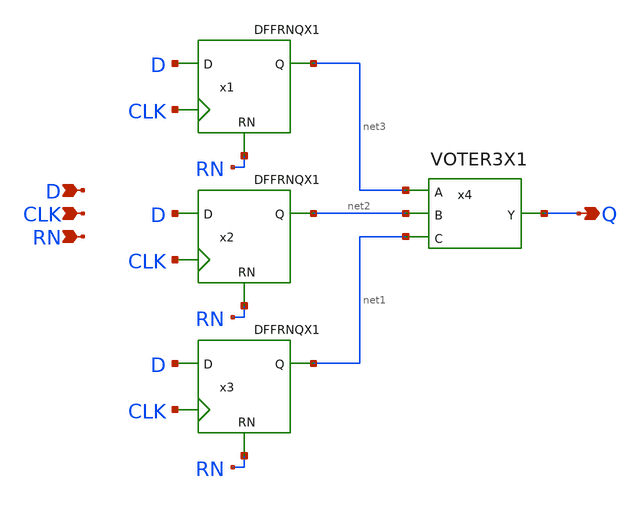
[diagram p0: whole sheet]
** sch_path: layout/xschem/sky130_rhbd/TMRDFFRNQX1.sch
**.subckt TMRDFFRNQX1 Q D CLK RN
*.opin Q
*.ipin D
*.ipin CLK
*.ipin RN
x1 net3 D CLK RN VDD VSS DFFRNQX1
x2 net2 D CLK RN VDD VSS DFFRNQX1
x3 net1 D CLK RN VDD VSS DFFRNQX1
x4 Q net3 net2 net1 VDD VSS VOTER3X1
**.ends
.end
